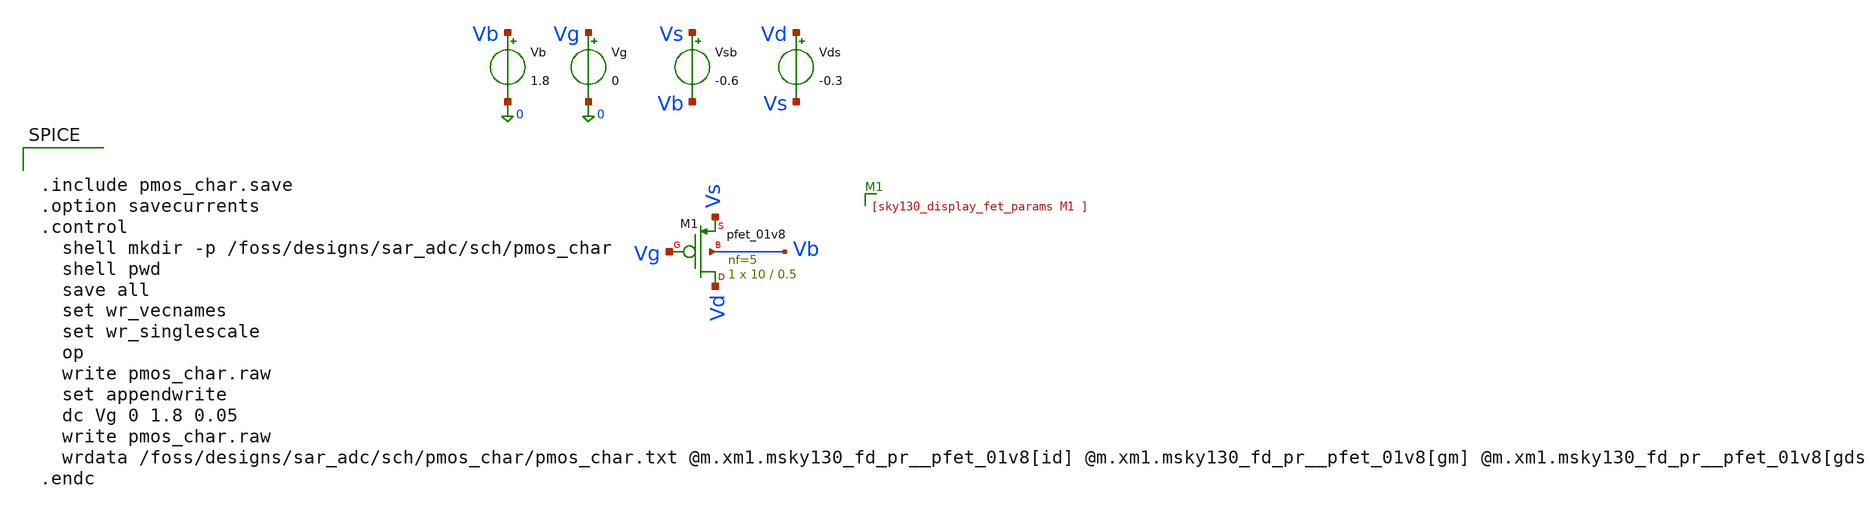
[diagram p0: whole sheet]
** sch_path: sch/archive/old/pmos_char.sch
**.subckt pmos_char
Vsb Vs Vb -0.6
.save i(vsb)
Vds Vd Vs -0.3
.save i(vds)
Vb Vb 0 1.8
.save i(vb)
Vg Vg 0 0
.save i(vg)
XM1 Vd Vg Vs Vb sky130_fd_pr__pfet_01v8 L=0.5 W=10 nf=5 ad='int((5 + 1)/2) * 10 / 5 * 0.29' as='int((5 + 2)/2) * 10 / 5 * 0.29'
+ pd='2*int((5 + 1)/2) * (10 / 5 + 0.29)' ps='2*int((5 + 2)/2) * (10 / 5 + 0.29)' nrd='0.29 / 10 ' nrs='0.29 / 10 '
+ sa=0 sb=0 sd=0 mult=1 m=1
**** begin user architecture code

** opencircuitdesign pdks install
.lib $::SKYWATER_MODELS/sky130.lib.spice tt
.include $::SKYWATER_STDCELLS/sky130_fd_sc_hd.spice



.include pmos_char.save
.option savecurrents
.control
  shell mkdir -p /foss/designs/sar_adc/sch/pmos_char
  shell pwd
  save all
  set wr_vecnames
  set wr_singlescale
  op
  write pmos_char.raw
  set appendwrite
  dc Vg 0 1.8 0.05
  write pmos_char.raw
  wrdata /foss/designs/sar_adc/sch/pmos_char/pmos_char.txt @m.xm1.msky130_fd_pr__pfet_01v8[id]
+ @m.xm1.msky130_fd_pr__pfet_01v8[gm] @m.xm1.msky130_fd_pr__pfet_01v8[gds]
.endc


**** end user architecture code
**.ends
.end
